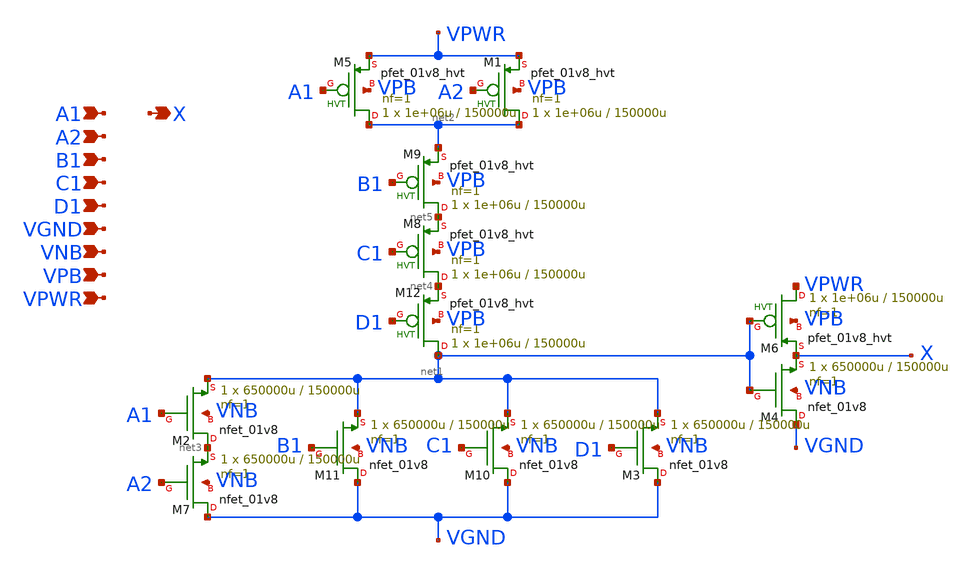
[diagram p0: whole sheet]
** sch_path: schematics/a2111o/sky130_fd_sc_hd__a2111o_1.sch
**.subckt sky130_fd_sc_hd__a2111o_1 A1 A2 B1 C1 D1 VGND VNB VPB VPWR X
*.ipin A1
*.ipin A2
*.ipin B1
*.ipin C1
*.ipin D1
*.ipin VGND
*.ipin VNB
*.ipin VPB
*.ipin VPWR
*.opin X
XM4 VGND net1 X VNB sky130_fd_pr__nfet_01v8 L=150000u W=650000u nf=1 ad='int((1 + 1)/2) * 650000u / 1 * 0.29'
+ as='int((1 + 2)/2) * 650000u / 1 * 0.29' pd='2*int((1 + 1)/2) * (650000u / 1 + 0.29)' ps='2*int((1 + 2)/2) * (650000u / 1 + 0.29)'
+ nrd='0.29 / 650000u ' nrs='0.29 / 650000u ' sa=0 sb=0 sd=0 mult=1 m=1
XM1 net2 A2 VPWR VPB sky130_fd_pr__pfet_01v8_hvt L=150000u W=1e+06u nf=1 ad='int((1 + 1)/2) * 1e+06u / 1 * 0.29'
+ as='int((1 + 2)/2) * 1e+06u / 1 * 0.29' pd='2*int((1 + 1)/2) * (1e+06u / 1 + 0.29)' ps='2*int((1 + 2)/2) * (1e+06u / 1 + 0.29)'
+ nrd='0.29 / 1e+06u ' nrs='0.29 / 1e+06u ' sa=0 sb=0 sd=0 mult=1 m=1
XM2 net3 A1 net1 VNB sky130_fd_pr__nfet_01v8 L=150000u W=650000u nf=1 ad='int((1 + 1)/2) * 650000u / 1 * 0.29'
+ as='int((1 + 2)/2) * 650000u / 1 * 0.29' pd='2*int((1 + 1)/2) * (650000u / 1 + 0.29)' ps='2*int((1 + 2)/2) * (650000u / 1 + 0.29)'
+ nrd='0.29 / 650000u ' nrs='0.29 / 650000u ' sa=0 sb=0 sd=0 mult=1 m=1
XM6 VPWR net1 X VPB sky130_fd_pr__pfet_01v8_hvt L=150000u W=1e+06u nf=1 ad='int((1 + 1)/2) * 1e+06u / 1 * 0.29'
+ as='int((1 + 2)/2) * 1e+06u / 1 * 0.29' pd='2*int((1 + 1)/2) * (1e+06u / 1 + 0.29)' ps='2*int((1 + 2)/2) * (1e+06u / 1 + 0.29)'
+ nrd='0.29 / 1e+06u ' nrs='0.29 / 1e+06u ' sa=0 sb=0 sd=0 mult=1 m=1
XM3 VGND D1 net1 VNB sky130_fd_pr__nfet_01v8 L=150000u W=650000u nf=1 ad='int((1 + 1)/2) * 650000u / 1 * 0.29'
+ as='int((1 + 2)/2) * 650000u / 1 * 0.29' pd='2*int((1 + 1)/2) * (650000u / 1 + 0.29)' ps='2*int((1 + 2)/2) * (650000u / 1 + 0.29)'
+ nrd='0.29 / 650000u ' nrs='0.29 / 650000u ' sa=0 sb=0 sd=0 mult=1 m=1
XM5 net2 A1 VPWR VPB sky130_fd_pr__pfet_01v8_hvt L=150000u W=1e+06u nf=1 ad='int((1 + 1)/2) * 1e+06u / 1 * 0.29'
+ as='int((1 + 2)/2) * 1e+06u / 1 * 0.29' pd='2*int((1 + 1)/2) * (1e+06u / 1 + 0.29)' ps='2*int((1 + 2)/2) * (1e+06u / 1 + 0.29)'
+ nrd='0.29 / 1e+06u ' nrs='0.29 / 1e+06u ' sa=0 sb=0 sd=0 mult=1 m=1
XM8 net4 C1 net5 VPB sky130_fd_pr__pfet_01v8_hvt L=150000u W=1e+06u nf=1 ad='int((1 + 1)/2) * 1e+06u / 1 * 0.29'
+ as='int((1 + 2)/2) * 1e+06u / 1 * 0.29' pd='2*int((1 + 1)/2) * (1e+06u / 1 + 0.29)' ps='2*int((1 + 2)/2) * (1e+06u / 1 + 0.29)'
+ nrd='0.29 / 1e+06u ' nrs='0.29 / 1e+06u ' sa=0 sb=0 sd=0 mult=1 m=1
XM9 net5 B1 net2 VPB sky130_fd_pr__pfet_01v8_hvt L=150000u W=1e+06u nf=1 ad='int((1 + 1)/2) * 1e+06u / 1 * 0.29'
+ as='int((1 + 2)/2) * 1e+06u / 1 * 0.29' pd='2*int((1 + 1)/2) * (1e+06u / 1 + 0.29)' ps='2*int((1 + 2)/2) * (1e+06u / 1 + 0.29)'
+ nrd='0.29 / 1e+06u ' nrs='0.29 / 1e+06u ' sa=0 sb=0 sd=0 mult=1 m=1
XM7 VGND A2 net3 VNB sky130_fd_pr__nfet_01v8 L=150000u W=650000u nf=1 ad='int((1 + 1)/2) * 650000u / 1 * 0.29'
+ as='int((1 + 2)/2) * 650000u / 1 * 0.29' pd='2*int((1 + 1)/2) * (650000u / 1 + 0.29)' ps='2*int((1 + 2)/2) * (650000u / 1 + 0.29)'
+ nrd='0.29 / 650000u ' nrs='0.29 / 650000u ' sa=0 sb=0 sd=0 mult=1 m=1
XM10 VGND C1 net1 VNB sky130_fd_pr__nfet_01v8 L=150000u W=650000u nf=1 ad='int((1 + 1)/2) * 650000u / 1 * 0.29'
+ as='int((1 + 2)/2) * 650000u / 1 * 0.29' pd='2*int((1 + 1)/2) * (650000u / 1 + 0.29)' ps='2*int((1 + 2)/2) * (650000u / 1 + 0.29)'
+ nrd='0.29 / 650000u ' nrs='0.29 / 650000u ' sa=0 sb=0 sd=0 mult=1 m=1
XM11 VGND B1 net1 VNB sky130_fd_pr__nfet_01v8 L=150000u W=650000u nf=1 ad='int((1 + 1)/2) * 650000u / 1 * 0.29'
+ as='int((1 + 2)/2) * 650000u / 1 * 0.29' pd='2*int((1 + 1)/2) * (650000u / 1 + 0.29)' ps='2*int((1 + 2)/2) * (650000u / 1 + 0.29)'
+ nrd='0.29 / 650000u ' nrs='0.29 / 650000u ' sa=0 sb=0 sd=0 mult=1 m=1
XM12 net1 D1 net4 VPB sky130_fd_pr__pfet_01v8_hvt L=150000u W=1e+06u nf=1 ad='int((1 + 1)/2) * 1e+06u / 1 * 0.29'
+ as='int((1 + 2)/2) * 1e+06u / 1 * 0.29' pd='2*int((1 + 1)/2) * (1e+06u / 1 + 0.29)' ps='2*int((1 + 2)/2) * (1e+06u / 1 + 0.29)'
+ nrd='0.29 / 1e+06u ' nrs='0.29 / 1e+06u ' sa=0 sb=0 sd=0 mult=1 m=1
**.ends
.end
